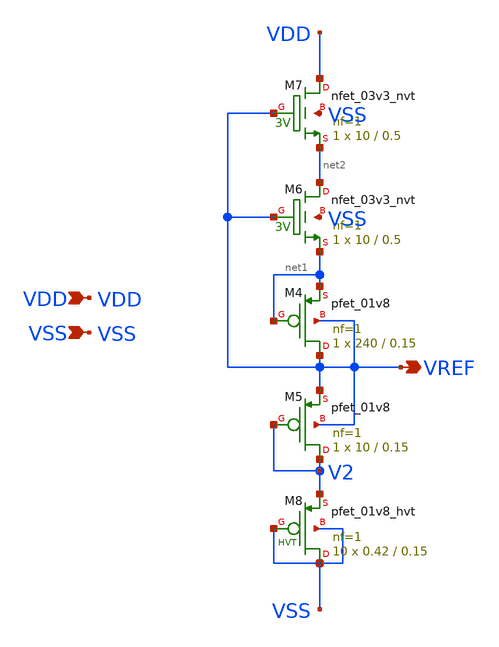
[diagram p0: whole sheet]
** sch_path: design/LELO_SVOD_SKY130A/LELO_SVOD_VTREF.sch
**.subckt LELO_SVOD_VTREF VDD VSS VREF
*.ipin VDD
*.ipin VSS
*.opin VREF
XM6 net2 VREF net1 VSS sky130_fd_pr__nfet_03v3_nvt L=0.5 W=10 nf=1 ad='int((1 + 1)/2) * 10 / 1 * 0.29'
+ as='int((1 + 2)/2) * 10 / 1 * 0.29' pd='2*int((1 + 1)/2) * (10 / 1 + 0.29)' ps='2*int((1 + 2)/2) * (10 / 1 + 0.29)'
+ nrd='0.29 / 10 ' nrs='0.29 / 10 ' sa=0 sb=0 sd=0 mult=1 m=1
XM7 VDD VREF net2 VSS sky130_fd_pr__nfet_03v3_nvt L=0.5 W=10 nf=1 ad='int((1 + 1)/2) * 10 / 1 * 0.29'
+ as='int((1 + 2)/2) * 10 / 1 * 0.29' pd='2*int((1 + 1)/2) * (10 / 1 + 0.29)' ps='2*int((1 + 2)/2) * (10 / 1 + 0.29)'
+ nrd='0.29 / 10 ' nrs='0.29 / 10 ' sa=0 sb=0 sd=0 mult=1 m=1
XM4 VREF net1 net1 VREF sky130_fd_pr__pfet_01v8 L=0.15 W=240 nf=1 ad='int((1 + 1)/2) * 240 / 1 * 0.29'
+ as='int((1 + 2)/2) * 240 / 1 * 0.29' pd='2*int((1 + 1)/2) * (240 / 1 + 0.29)' ps='2*int((1 + 2)/2) * (240 / 1 + 0.29)'
+ nrd='0.29 / 240 ' nrs='0.29 / 240 ' sa=0 sb=0 sd=0 mult=1 m=1
XM5 V2 V2 VREF VREF sky130_fd_pr__pfet_01v8 L=0.15 W=10 nf=1 ad='int((1 + 1)/2) * 10 / 1 * 0.29' as='int((1 + 2)/2) * 10 / 1 * 0.29'
+ pd='2*int((1 + 1)/2) * (10 / 1 + 0.29)' ps='2*int((1 + 2)/2) * (10 / 1 + 0.29)' nrd='0.29 / 10 ' nrs='0.29 / 10 '
+ sa=0 sb=0 sd=0 mult=1 m=1
XM8 VSS VSS V2 VSS sky130_fd_pr__pfet_01v8_hvt L=0.15 W=0.42 nf=1 ad='int((1 + 1)/2) * 0.42 / 1 * 0.29'
+ as='int((1 + 2)/2) * 0.42 / 1 * 0.29' pd='2*int((1 + 1)/2) * (0.42 / 1 + 0.29)' ps='2*int((1 + 2)/2) * (0.42 / 1 + 0.29)'
+ nrd='0.29 / 0.42 ' nrs='0.29 / 0.42 ' sa=0 sb=0 sd=0 mult=10 m=10
**.ends
.end
